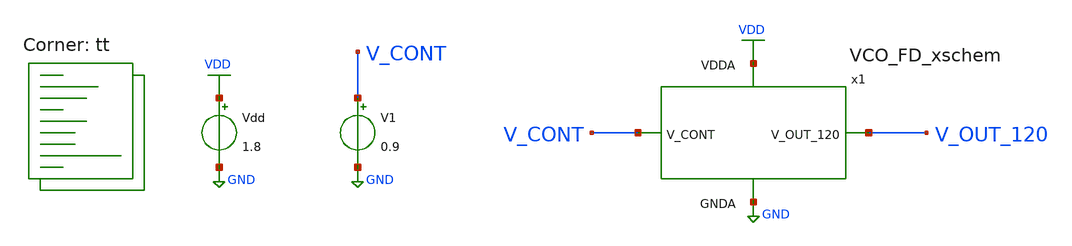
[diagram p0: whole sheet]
** sch_path: projects/pll/vco/magic/tb_current_starved_VCO_FD_xschem.sch
**.subckt tb_current_starved_VCO_FD_xschem
Vdd VDD GND 1.8
V1 V_CONT GND 0.9
x1 V_OUT_120 VDD GND V_CONT VCO_FD_xschem
**** begin user architecture code
.lib $::SKYWATER_MODELS/sky130.lib.spice tt



.include /foss/designs/my_design/projects/pll/vco/magic/VCO_FD_magic.spice

.option method=trap
.option wnflag=1

.control

  let v_cont_start = 0.0
  let v_cont_stop = 1.9

  dowhile v_cont_start <= v_cont_stop
    alter v1 $&v_cont_start
    * save v(v_osc) v(v_cont) v(v_out)
    save all
    tran 5ps 30ns
    remzerovec
    write tb_current_starved_VCO_FD_xschem_{$&v_cont_start}.raw
    * write tb_current_starved_VCO_FD_xschem.raw
    linearize v(v_osc)
    let filename = v_cont_start * 100
    wrdata /foss/designs/my_design/projects/pll/vco/magic/tb_current_starved_VCO_FD_xschem_{$&filename}.txt
+ v(v_osc)
    * wrdata /foss/designs/my_design/projects/pll/vco/magic/tb_current_starved_VCO_FD_xschem.txt
+ v(v_osc)
    set appendwrite

    reset
    let v_cont_start = v_cont_start + 0.1
   end
.endc



**** end user architecture code
**.ends
.GLOBAL GND
.GLOBAL VDD
.end
